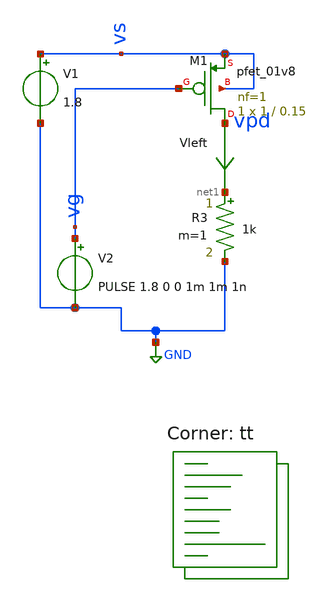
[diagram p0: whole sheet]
** sch_path: Schematics/mos_resistors/ig_mpos.sch
**.subckt ig_mpos
V1 vs GND 1.8
.save i(v1)
V2 vg GND PULSE 1.8 0 0 1m 1m 1n
.save i(v2)
XM1 vpd vg vs vs sky130_fd_pr__pfet_01v8 L=0.15 W=1 nf=1 ad='int((nf+1)/2) * W/nf * 0.29' as='int((nf+2)/2) * W/nf * 0.29'
+ pd='2*int((nf+1)/2) * (W/nf + 0.29)' ps='2*int((nf+2)/2) * (W/nf + 0.29)' nrd='0.29 / W' nrs='0.29 / W'
+ sa=0 sb=0 sd=0 mult=1 m=1
Vleft vpd net1 0
.save i(vleft)
R3 net1 GND 1k m=1
**** begin user architecture code
.lib $::SKYWATER_MODELS/sky130.lib.spice tt
**** end user architecture code
**.ends
.GLOBAL GND
**** begin user architecture code

*.options savecurrents
.tran 10u 2m
.save all
.control
	run
	write ig_mpos.raw
.endc


**** end user architecture code
.end
